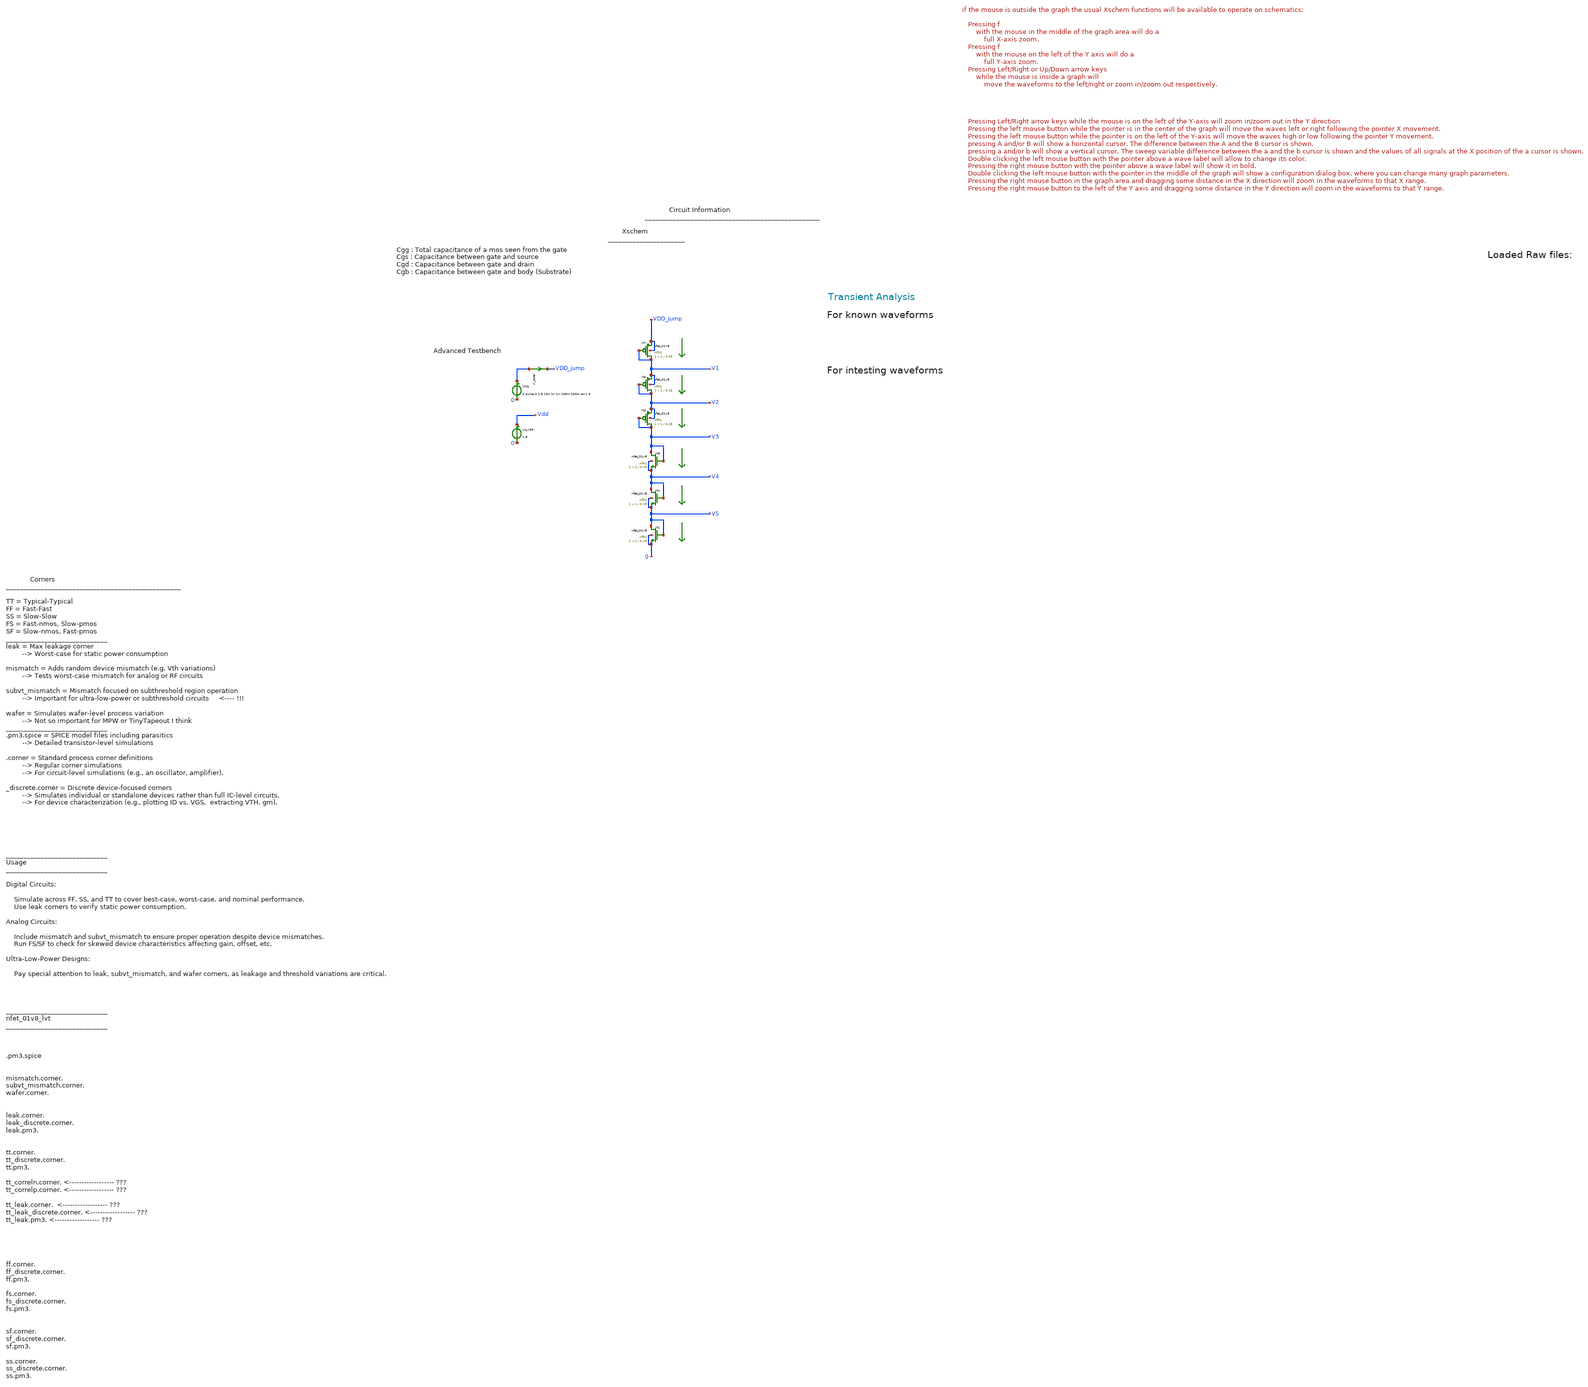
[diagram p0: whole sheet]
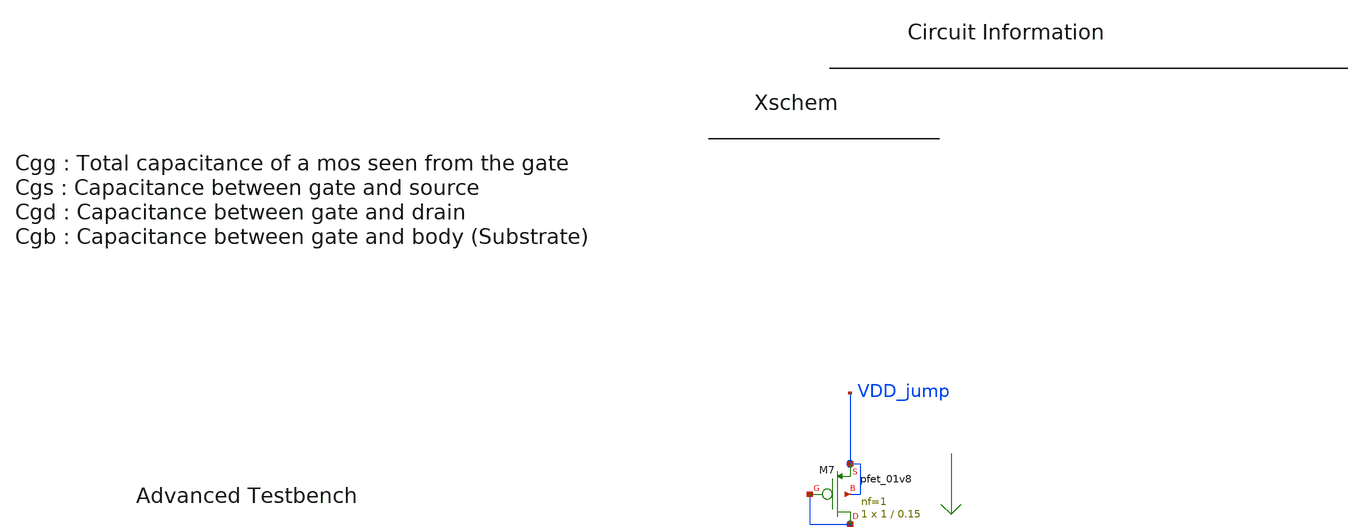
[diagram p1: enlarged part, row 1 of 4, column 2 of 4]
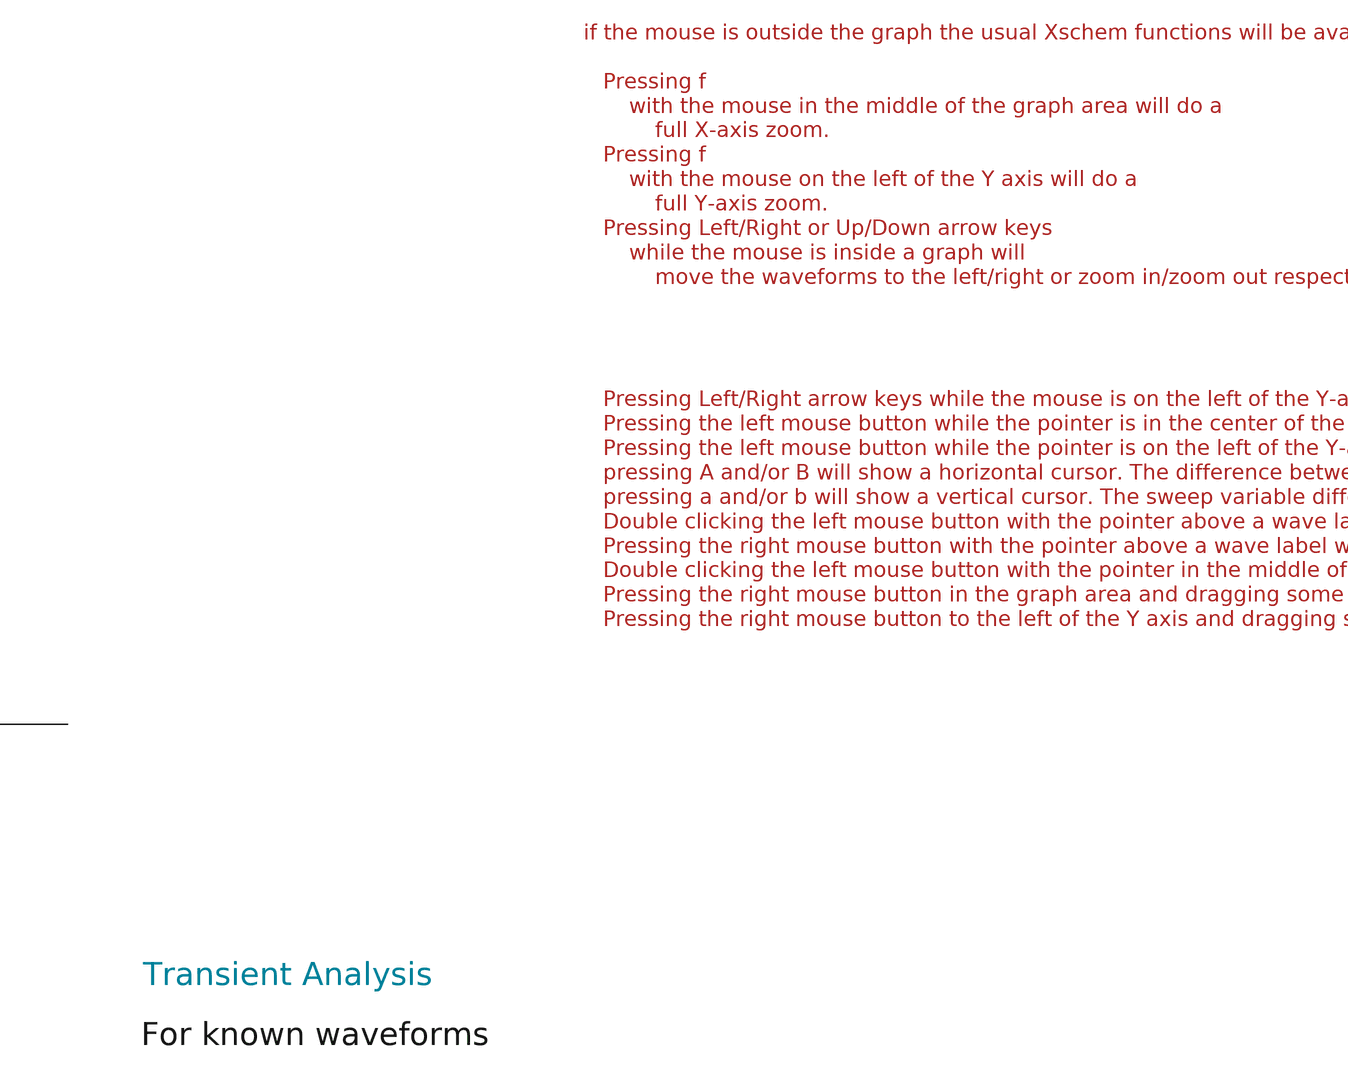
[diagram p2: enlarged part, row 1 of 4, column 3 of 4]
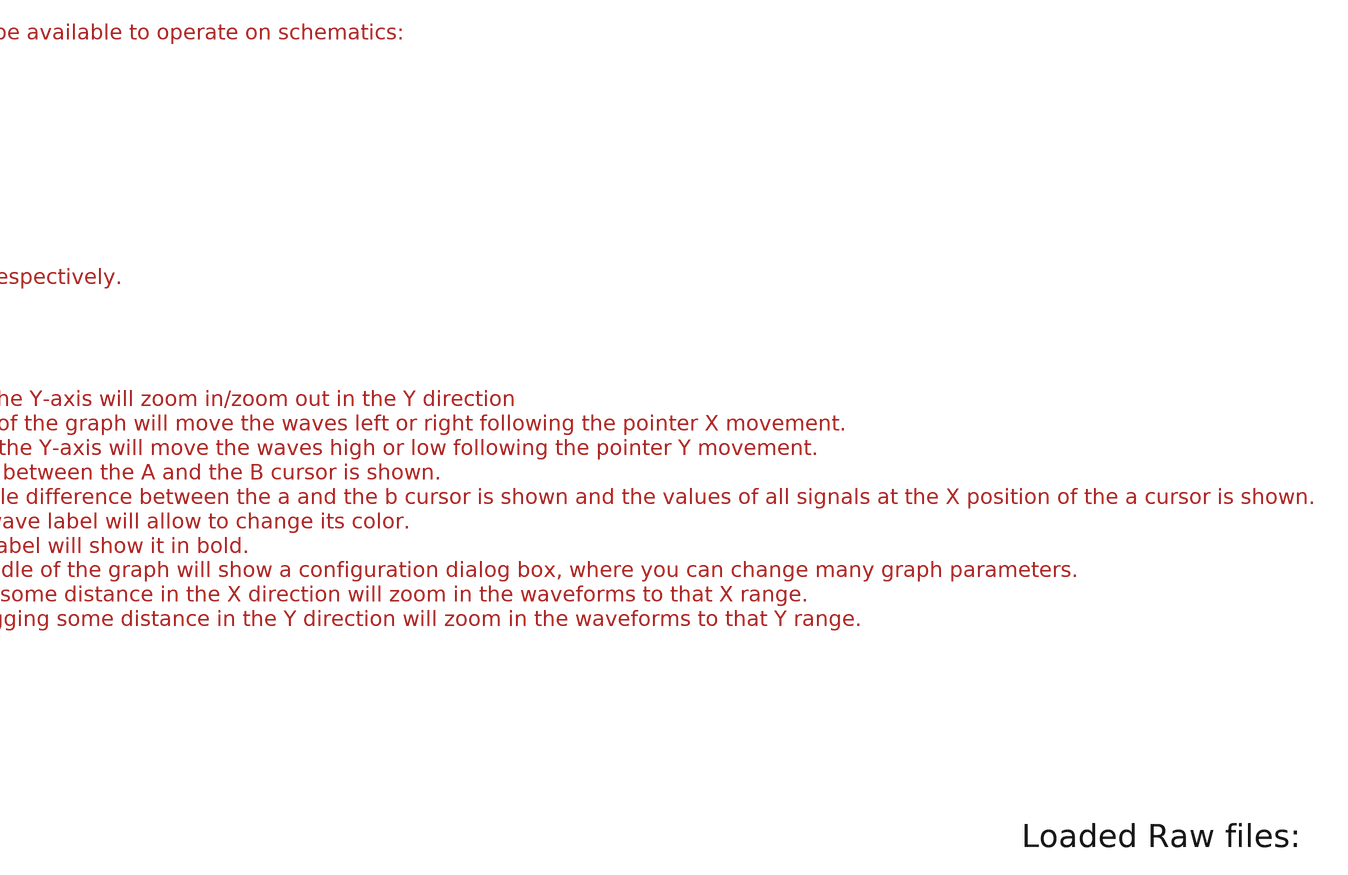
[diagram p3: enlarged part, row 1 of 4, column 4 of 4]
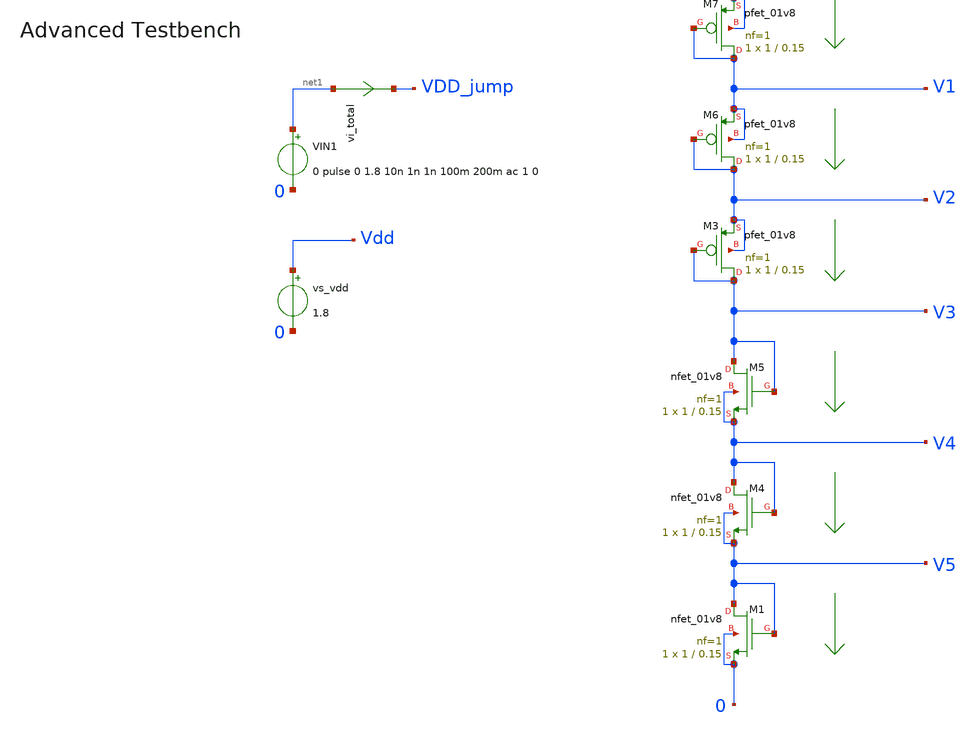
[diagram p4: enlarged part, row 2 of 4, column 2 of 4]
** sch_path: tt10-hdl/tt_um_test_commit/xschem/T2/startup/POR/A_tt10_biasCurrCap/POR_tb.sch
* Copyright (C) 1998-2024 Stefan Frederik Schippers
* This program is free software; you can redistribute it and/or modify
* it under the terms of the GNU General Public License as published by
* the Free Software Foundation; either version 2 of the License, or
* (at your option) any later version.
* This program is distributed in the hope that it will be useful,
* but WITHOUT ANY WARRANTY; without even the implied warranty of
* MERCHANTABILITY or FITNESS FOR A PARTICULAR PURPOSE.  See the
* GNU General Public License for more details.
* You should have received a copy of the GNU General Public License
* along with this program; if not, write to the Free Software
**.subckt POR_tb
VIN1 net1 0 0 pulse 0 1.8 10n 1n 1n 100m 200m ac 1 0
vi_total net1 VDD_jump 0
.save i(vi_total)
vs_vdd Vdd 0 1.8
XM1 V5 V5 0 0 sky130_fd_pr__nfet_01v8 L=0.15 W=1 nf=1 ad='int((1 + 1)/2) * 1 / 1 * 0.29' as='int((1 + 2)/2) * 1 / 1 * 0.29'
+ pd='2*int((1 + 1)/2) * (1 / 1 + 0.29)' ps='2*int((1 + 2)/2) * (1 / 1 + 0.29)' nrd='0.29 / 1 ' nrs='0.29 / 1 '
+ sa=0 sb=0 sd=0 mult=1 m=1
XM3 V3 V3 V2 V2 sky130_fd_pr__pfet_01v8 L=0.15 W=1 nf=1 ad='int((nf+1)/2) * W/nf * 0.29' as='int((nf+2)/2) * W/nf * 0.29'
+ pd='2*int((nf+1)/2) * (W/nf + 0.29)' ps='2*int((nf+2)/2) * (W/nf + 0.29)' nrd='0.29 / W' nrs='0.29 / W'
+ sa=0 sb=0 sd=0 mult=1 m=1
XM4 V4 V4 V5 V5 sky130_fd_pr__nfet_01v8 L=0.15 W=1 nf=1 ad='int((1 + 1)/2) * 1 / 1 * 0.29' as='int((1 + 2)/2) * 1 / 1 * 0.29'
+ pd='2*int((1 + 1)/2) * (1 / 1 + 0.29)' ps='2*int((1 + 2)/2) * (1 / 1 + 0.29)' nrd='0.29 / 1 ' nrs='0.29 / 1 '
+ sa=0 sb=0 sd=0 mult=1 m=1
XM5 V3 V3 V4 V4 sky130_fd_pr__nfet_01v8 L=0.15 W=1 nf=1 ad='int((1 + 1)/2) * 1 / 1 * 0.29' as='int((1 + 2)/2) * 1 / 1 * 0.29'
+ pd='2*int((1 + 1)/2) * (1 / 1 + 0.29)' ps='2*int((1 + 2)/2) * (1 / 1 + 0.29)' nrd='0.29 / 1 ' nrs='0.29 / 1 '
+ sa=0 sb=0 sd=0 mult=1 m=1
XM6 V2 V2 V1 V1 sky130_fd_pr__pfet_01v8 L=0.15 W=1 nf=1 ad='int((nf+1)/2) * W/nf * 0.29' as='int((nf+2)/2) * W/nf * 0.29'
+ pd='2*int((nf+1)/2) * (W/nf + 0.29)' ps='2*int((nf+2)/2) * (W/nf + 0.29)' nrd='0.29 / W' nrs='0.29 / W'
+ sa=0 sb=0 sd=0 mult=1 m=1
XM7 V1 V1 VDD_jump VDD_jump sky130_fd_pr__pfet_01v8 L=0.15 W=1 nf=1 ad='int((nf+1)/2) * W/nf * 0.29'
+ as='int((nf+2)/2) * W/nf * 0.29' pd='2*int((nf+1)/2) * (W/nf + 0.29)' ps='2*int((nf+2)/2) * (W/nf + 0.29)'
+ nrd='0.29 / W' nrs='0.29 / W' sa=0 sb=0 sd=0 mult=1 m=1
**** begin user architecture code



.temp 30

*.option gmin=5n
*.option scale=1e-6
.option wnflag=1
.option savecurrents

.save all
.control
  save all alli
  save @m.xm1.msky130_fd_pr__nfet_01v8[gm]
  save @m.xm1.msky130_fd_pr__nfet_01v8[id]
  save @m.xm1.msky130_fd_pr__nfet_01v8[vgs]

  save @m.xm1.msky130_fd_pr__nfet_01v8[cgg]
  save @m.xm1.msky130_fd_pr__nfet_01v8[cgs]
  save @m.xm1.msky130_fd_pr__nfet_01v8[cgdo]
  save @m.xm1.msky130_fd_pr__nfet_01v8[cgb]

  save @m.xm1.msky130_fd_pr__nfet_01v8[vds]
  save @m.xm1.msky130_fd_pr__nfet_01v8[vdsat]
  save @m.xm1.msky130_fd_pr__nfet_01v8[vth]


  save @m.xm1.msky130_fd_pr__nfet_01v8[leff]
  save @m.xm1.msky130_fd_pr__nfet_01v8[weff]
  save @m.xm1.msky130_fd_pr__nfet_01v8[gds]
  save @m.xm1.msky130_fd_pr__nfet_01v8[l]
  save @m.xm1.msky130_fd_pr__nfet_01v8[w]
  save @m.xm1.msky130_fd_pr__nfet_01v8[gm]
  save @m.xm1.msky130_fd_pr__nfet_01v8[gm]
  save @m.xm1.msky130_fd_pr__nfet_01v8[gm]
  save @m.xm1.msky130_fd_pr__nfet_01v8[gm]
  save @m.xm1.msky130_fd_pr__nfet_01v8[gm]




  *dc v_dev_vds 0 1.8 0.005 v_dev_vgs 0 1.8 0.2
  *write nmos_tb.raw




  tran 10u 10m
  write nmos_tb_tran.raw

  op
  set appendwrite
  write nmos_tb_tran.raw






  *quit 0




.endc





** opencircuitdesign pdks install
.lib $::SKYWATER_MODELS/sky130.lib.spice tt
.include $::SKYWATER_STDCELLS/sky130_fd_sc_hd.spice


**** end user architecture code
**.ends
.end
